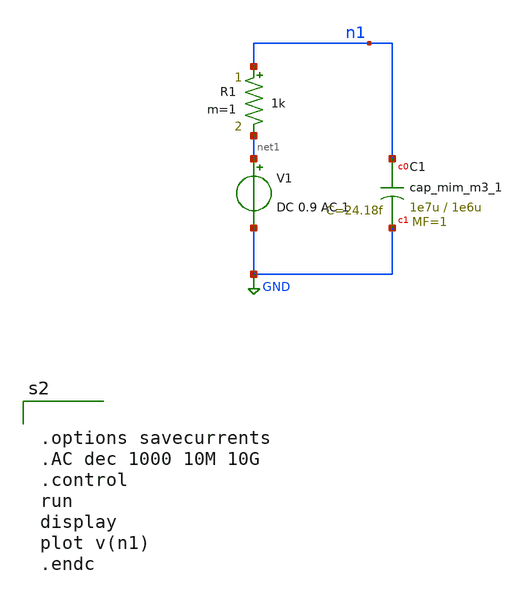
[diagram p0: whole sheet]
** sch_path: xschem/untitled-9.sch
**.subckt untitled-9
V1 net1 GND DC 0.9 AC 1
R1 n1 net1 1k m=1
XC1 n1 GND sky130_fd_pr__cap_mim_m3_1 W=1e7u L=1e6u MF=1 m=1
**** begin user architecture code
.lib $::SKYWATER_MODELS/sky130.lib.spice ff
* .include $::PDKPATH/libs.ref/sky130_fd_sc_hvl/spice/sky130_fd_sc_hvl.spice



.options savecurrents
.AC dec 1000 10M 10G
.control
run
display
plot v(n1)
.endc


**** end user architecture code
**.ends
.GLOBAL GND
.end
